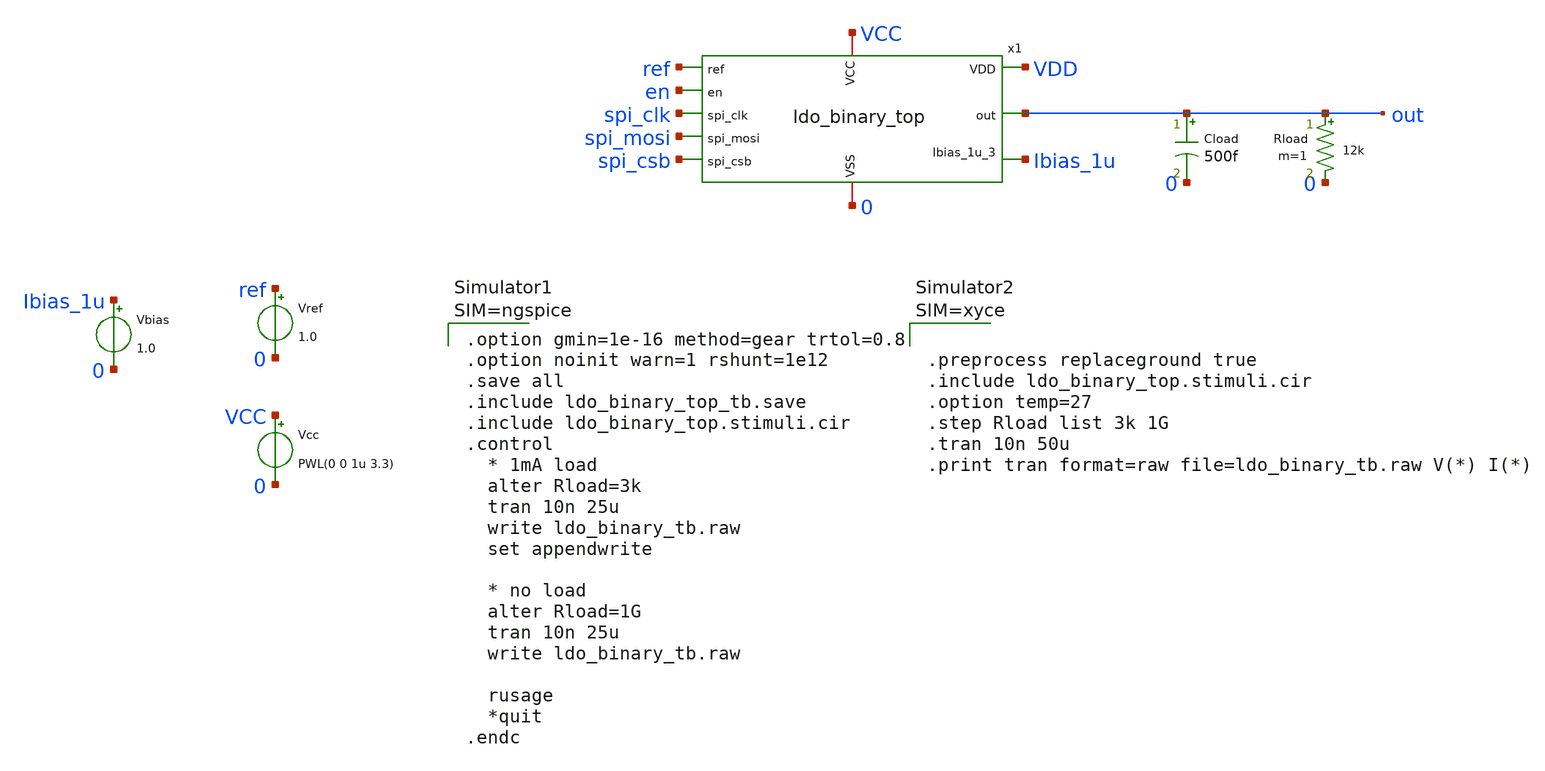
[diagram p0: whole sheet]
** sch_path: FLDO/design_data/xschem/ldo_binary_top_tb.sch
* IHP-GmbH/IHP-Open-PDK/ihp-sg13g2/libs.tech/xschem/sg13g2_stdcells/sg13g2_decap_4.sch:
* Copyright 2023 IHP PDK Authors
* Licensed under the Apache License, Version 2.0 (the "License");
**.subckt ldo_binary_top_tb
x1 VCC 0 spi_clk spi_mosi spi_csb ref en out Ibias_1u VDD ldo_binary_top
Vcc VCC 0 PWL(0 0 1u 3.3)
Vref ref 0 1.0
Cload out 0 500f m=1
Rload out 0 12k m=1
Vbias Ibias_1u 0 1.0
**** begin user architecture code









** IHP models
.lib cornerMOSlv.lib mos_tt
.lib cornerMOShv.lib mos_tt
.lib cornerHBT.lib hbt_typ
.lib cornerRES.lib res_typ
.lib cornerCAP.lib cap_typ

.include sg13g2_stdcell.spice






.option gmin=1e-16 method=gear trtol=0.8
.option noinit warn=1 rshunt=1e12
.save all
.include ldo_binary_top_tb.save
.include ldo_binary_top.stimuli.cir
.control
  * 1mA load
  alter Rload=3k
  tran 10n 25u
  write ldo_binary_tb.raw
  set appendwrite

  * no load
  alter Rload=1G
  tran 10n 25u
  write ldo_binary_tb.raw

  rusage
  *quit
.endc



**** end user architecture code
**.ends

* expanding   symbol:  ldo_binary_top.sym # of pins=10
** sym_path: FLDO/design_data/xschem/ldo_binary_top.sym
** sch_path: FLDO/design_data/xschem/ldo_binary_top.sch
.subckt ldo_binary_top VCC VSS spi_clk spi_mosi spi_csb ref en out Ibias_1u_3 VDD
*.iopin VCC
*.ipin spi_clk
*.iopin VSS
*.opin out
*.ipin spi_mosi
*.ipin spi_csb
*.ipin ref
*.ipin en
*.opin Ibias_1u_3
*.opin VDD
x_shift3 VCC VDD VSS a3 a3_hv shifter
x_shift2 VCC VDD VSS a2 a2_hv shifter
x_shift1 VCC VDD VSS a1 a1_hv shifter
x_shift0 VCC VDD VSS a0 a0_hv shifter
x1 VCC VSS ref Ibias_1u_1 out a3_hv a2_hv a1_hv a0_hv net1 ldo_binary
x3 VCC VSS ref Ibias_1u_2 VDD por ldo_1v2
x4 VCC VSS Ibias_1u_1 Ibias_1u_2 Ibias_1u_3 por biasgen
x2 VDD VSS spi_clk spi_mosi spi_csb por en a3 a2 a1 a0 en_ldo_n ldo_control
x_shift_enable VCC VDD VSS en_ldo_n net1 shifter
.ends


* expanding   symbol:  shifter.sym # of pins=5
** sym_path: FLDO/design_data/xschem/shifter.sym
** sch_path: FLDO/design_data/xschem/shifter.sch
.subckt shifter VDD_3v3 VDD_1v2 GND in out
*.iopin VDD_3v3
*.iopin VDD_1v2
*.iopin GND
*.ipin in
*.opin out
XM1 lvlsh in_b GND GND sg13_hv_nmos w=2u l=0.45u ng=1 m=1 mm_ok=1
XM2 lvlsh_b in GND GND sg13_hv_nmos w=2u l=0.45u ng=1 m=1 mm_ok=1
XM3 lvlsh lvlsh_b VDD_3v3 VDD_3v3 sg13_hv_pmos w=0.3u l=0.45u ng=1 m=1 mm_ok=1
XM4 lvlsh_b lvlsh VDD_3v3 VDD_3v3 sg13_hv_pmos w=0.3u l=0.45u ng=1 m=1 mm_ok=1
XM5 in_b in GND GND sg13_lv_nmos w=0.74u l=0.13u ng=1 m=1 mm_ok=1
XM6 in_b in VDD_1v2 VDD_1v2 sg13_lv_pmos w=1.12u l=0.13u ng=1 m=1 mm_ok=1
XM7 out lvlsh_b GND GND sg13_hv_nmos w=2u l=0.45u ng=1 m=1 mm_ok=1
XM8 out lvlsh_b VDD_3v3 VDD_3v3 sg13_hv_pmos w=2u l=0.4u ng=1 m=2 mm_ok=1
.ends


* expanding   symbol:  ldo_binary.sym # of pins=7
** sym_path: FLDO/design_data/xschem/ldo_binary.sym
** sch_path: FLDO/design_data/xschem/ldo_binary.sch
.subckt ldo_binary VCC GND ref Ibias_1u out a3 a2 a1 a0 en_n
*.iopin VCC
*.iopin GND
*.ipin ref
*.ipin Ibias_1u
*.opin out
*.ipin a3,a2,a1,a0
*.ipin en_n
XR4 net1 out GND rhigh w=0.5e-6 l=12e-6 m=1 b=0
XM1 net1 a0 out VCC sg13_hv_pmos w=2u l=0.4u ng=1 m=1 mm_ok=1
XM2 net2 a1 net1 VCC sg13_hv_pmos w=2u l=0.4u ng=1 m=1 mm_ok=1
XM3 net3 a2 net2 VCC sg13_hv_pmos w=2u l=0.4u ng=1 m=1 mm_ok=1
XM4 out vg net4 net4 sg13_hv_pmos w=100u l=0.4u ng=10 m=1 mm_ok=1
Vmeas VCC net4 0
.save i(vmeas)
XC1 out vg cap_cmim w=10.0e-6 l=10.0e-6 m=1
XM11 net5 a3 net3 VCC sg13_hv_pmos w=2u l=0.4u ng=1 m=1 mm_ok=1
XM15 vg en VCC VCC sg13_hv_pmos w=0.3u l=0.4u ng=1 m=1 mm_ok=1
x1 VCC GND Ibias_1u fb ref vg ldo_ota
XM5 Ibias_1u en_n GND GND sg13_hv_nmos w=0.3u l=0.45u ng=1 m=1 mm_ok=1
XM6 en en_n GND GND sg13_hv_nmos w=0.3u l=0.45u ng=1 m=1 mm_ok=1
XM7 en en_n VCC VCC sg13_hv_pmos w=0.3u l=0.4u ng=1 m=1 mm_ok=1
XRdummy GND GND gnd rhigh w=0.5e-6 l=12e-6 m=5 b=0
XR2 net2 net1 GND rhigh w=0.5e-6 l=2*12e-6 m=1 b=0
XR6 net3 net2 GND rhigh w=0.5e-6 l=4*12e-6 m=1 b=0
XR5 net5 net3 GND rhigh w=0.5e-6 l=8*12e-6 m=1 b=0
XR3 fb net5 GND rhigh w=0.5e-6 l=6*12e-6 m=1 b=0
XR1 GND fb GND rhigh w=0.5e-6 l=10*12e-6 m=1 b=0
.ends


* expanding   symbol:  ldo_1v2.sym # of pins=6
** sym_path: FLDO/design_data/xschem/ldo_1v2.sym
** sch_path: FLDO/design_data/xschem/ldo_1v2.sch
.subckt ldo_1v2 VCC GND ref Ibias_1u out en_n
*.iopin VCC
*.iopin GND
*.ipin ref
*.ipin Ibias_1u
*.opin out
*.ipin en_n
XM4 out vg net1 net1 sg13_hv_pmos w=50u l=0.4u ng=10 m=1 mm_ok=1
Vmeas VCC net1 0
.save i(vmeas)
XC1 out vg cap_cmim w=10.0e-6 l=10.0e-6 m=1
XM2 Ibias_1u en_n GND GND sg13_hv_nmos w=0.3u l=0.45u ng=1 m=1 mm_ok=1
XM3 vg en VCC VCC sg13_hv_pmos w=0.3u l=0.4u ng=1 m=1 mm_ok=1
XM1 en en_n GND GND sg13_hv_nmos w=0.3u l=0.45u ng=1 m=1 mm_ok=1
XM11 en en_n VCC VCC sg13_hv_pmos w=0.3u l=0.4u ng=1 m=1 mm_ok=1
XRdummy GND GND gnd rhigh w=0.5e-6 l=4e-6 m=2 b=0 mm_ok=1
x1 VCC GND Ibias_1u fb ref vg ldo_ota
XR2 fb out gnd rhigh w=0.5e-6 l=4*4e-6 m=1 b=0
XR1 GND fb gnd rhigh w=0.5e-6 l=20*4e-6 m=1 b=0
.ends


* expanding   symbol:  biasgen.sym # of pins=4
** sym_path: FLDO/design_data/xschem/biasgen.sym
** sch_path: FLDO/design_data/xschem/biasgen.sch
.subckt biasgen VCC GND Ibias_1u_1 Ibias_1u_2 Ibias_1u_3 por
*.iopin VCC
*.iopin GND
*.iopin Ibias_1u_1,Ibias_1u_2,Ibias_1u_3
*.opin por
XM1 vp vn net1 GND sg13_hv_nmos w=2u l=2u ng=1 m=3 mm_ok=1
XM2 vn vn GND GND sg13_hv_nmos w=2u l=2u ng=1 m=1 mm_ok=1
XM3 vn vp VCC VCC sg13_hv_pmos w=0.5u l=2u ng=1 m=2 mm_ok=1
XM4 vp vp VCC VCC sg13_hv_pmos w=0.5u l=2u ng=1 m=2 mm_ok=1
XMout0 Ibias_1u_0 vp VCC VCC sg13_hv_pmos w=0.5u l=2u ng=1 m=1 mm_ok=1
XMout1 Ibias_1u_1 vp VCC VCC sg13_hv_pmos w=0.5u l=2u ng=1 m=1 mm_ok=1
XMout2 Ibias_1u_2 vp VCC VCC sg13_hv_pmos w=0.5u l=2u ng=1 m=1 mm_ok=1
XMout3 Ibias_1u_3 vp VCC VCC sg13_hv_pmos w=0.5u l=2u ng=1 m=1 mm_ok=1
XC1 Ibias_1u_0 GND cap_cmim w=7.0e-6 l=7.0e-6 m=1
XM7 por Ibias_1u_0 VCC VCC sg13_hv_pmos w=0.3u l=0.4u ng=1 m=1 mm_ok=1
XM8 por Ibias_1u_0 GND GND sg13_hv_nmos w=0.3u l=0.45u ng=1 m=1 mm_ok=1
XR1 net1 GND GND rppd w=0.5e-6 l=80e-6 m=1 b=0 mm_ok=1
XM5 vp vstart GND GND sg13_hv_nmos w=0.3u l=0.45u ng=1 m=1 mm_ok=1
XM6 vstart vn GND GND sg13_hv_nmos w=0.3u l=0.45u ng=1 m=1 mm_ok=1
XM9 vstart vn net2 VCC sg13_hv_pmos w=0.3u l=2u ng=1 m=1 mm_ok=1
XM10 net2 net2 net3 VCC sg13_hv_pmos w=0.3u l=2u ng=1 m=1 mm_ok=1
XM11 net3 net3 VCC VCC sg13_hv_pmos w=0.3u l=2u ng=1 m=1 mm_ok=1
.ends


* expanding   symbol:  ldo_control.sym # of pins=9
** sym_path: FLDO/design_data/xschem/ldo_control.sym
** sch_path: FLDO/design_data/xschem/ldo_control.sch
.subckt ldo_control VDD VSS spi_clk spi_di spi_ce por en data3 data2 data1 data0 en_ldo_n
*.iopin VDD
*.ipin spi_clk
*.iopin VSS
*.opin data3,data2,data1,data0
*.ipin spi_di
*.ipin spi_ce
*.ipin por
*.ipin en
*.opin en_ldo_n
x1 VDD VSS spi_clk spi_di spi_ce rst_b data3 data2 data1 data0 spi_register
x2 en_ldo_n rst_b en VDD VSS sg13g2_nand2_1
x3 rst_b por VDD VSS shifter_down_invert
x4 VDD VSS sg13g2_decap_4
x5 VDD VSS sg13g2_decap_4
x6 VDD VSS sg13g2_decap_8
x7 VDD VSS sg13g2_decap_8
x8 VDD VSS sg13g2_decap_8
x9 VDD VSS sg13g2_fill_2
.ends


* expanding   symbol:  ldo_ota.sym # of pins=6
** sym_path: FLDO/design_data/xschem/ldo_ota.sym
** sch_path: FLDO/design_data/xschem/ldo_ota.sch
.subckt ldo_ota VCC GND Ibias_1u plus min out
*.iopin VCC
*.iopin GND
*.ipin plus
*.ipin min
*.opin out
*.ipin Ibias_1u
XM5 vbp plus tail GND sg13_hv_nmos w=3u l=2u ng=3 m=1 mm_ok=1
XM6 out min tail GND sg13_hv_nmos w=3u l=2u ng=3 m=1 mm_ok=1
XM7 tail Ibias_1u GND GND sg13_hv_nmos w=1u l=2u ng=1 m=2 mm_ok=1
XM8 Ibias_1u Ibias_1u GND GND sg13_hv_nmos w=1u l=2u ng=1 m=1 mm_ok=1
XM9 out vbp VCC VCC sg13_hv_pmos w=2u l=2u ng=2 m=1 mm_ok=1
XM10 vbp vbp VCC VCC sg13_hv_pmos w=2u l=2u ng=2 m=1 mm_ok=1
XMdummy0 GND Ibias_1u GND GND sg13_hv_nmos w=1u l=2u ng=1 m=2 mm_ok=1
XMdummy1 tail tail tail GND sg13_hv_nmos w=1u l=2u ng=1 m=4 mm_ok=1
XMdummyP VCC vbp VCC VCC sg13_hv_pmos w=1u l=2u ng=1 m=2 mm_ok=1
.ends


* expanding   symbol:  spi_register.sym # of pins=7
** sym_path: FLDO/design_data/xschem/spi_register.sym
** sch_path: FLDO/design_data/xschem/spi_register.sch
.subckt spi_register VDD VSS spi_clk spi_di spi_ce rst_b data3 data2 data1 data0
*.iopin VDD
*.ipin spi_clk
*.iopin VSS
*.opin data3,data2,data1,data0
*.ipin spi_di
*.ipin spi_ce
*.ipin rst_b
xshift3 shiftreg3 net2[3] net1 shiftreg2 rst_b VDD VSS sg13g2_dfrbp_1
xshift2 shiftreg2 net2[2] net1 shiftreg1 rst_b VDD VSS sg13g2_dfrbp_1
xshift1 shiftreg1 net2[1] net1 shiftreg0 rst_b VDD VSS sg13g2_dfrbp_1
xshift0 shiftreg0 net2[0] net1 spi_di rst_b VDD VSS sg13g2_dfrbp_1
x2 net1 spi_clk spi_ce VDD VSS sg13g2_nor2_1
xdata3 shiftreg3 rst_b VGND VNB VPB VPWR data3 sg13g2_dlhrq_1
xdata2 shiftreg2 rst_b VGND VNB VPB VPWR data2 sg13g2_dlhrq_1
xdata1 shiftreg1 rst_b VGND VNB VPB VPWR data1 sg13g2_dlhrq_1
xdata0 shiftreg0 rst_b VGND VNB VPB VPWR data0 sg13g2_dlhrq_1
* noconn #net2
.ends


* expanding   symbol:  sg13g2_stdcells/sg13g2_nand2_1.sym # of pins=3
** sym_path: sg13g2_stdcells/sg13g2_nand2_1.sym
** sch_path: sg13g2_stdcells/sg13g2_nand2_1.sch
.subckt sg13g2_nand2_1 Y A B VDD VSS
*.iopin VDD
*.iopin VSS
*.ipin A
*.ipin B
*.opin Y
XM1 Y A net1 VSS sg13_lv_nmos w=740.00n l=130.00n ng=1 m=1 mm_ok=1
XM2 net1 B VSS VSS sg13_lv_nmos w=740.00n l=130.00n ng=1 m=1 mm_ok=1
XM3 Y A VDD VDD sg13_lv_pmos w=1.12u l=130.00n ng=1 m=1 mm_ok=1
XM4 Y B VDD VDD sg13_lv_pmos w=1.12u l=130.00n ng=1 m=1 mm_ok=1
.ends


* expanding   symbol:  shifter_down_invert.sym # of pins=2
** sym_path: FLDO/design_data/xschem/shifter_down_invert.sym
** sch_path: FLDO/design_data/xschem/shifter_down_invert.sch
.subckt shifter_down_invert Y A VDD VSS
*.opin Y
*.ipin A
XM1 Y A VSS VSS sg13_hv_nmos w=0.3u l=0.45u ng=1 m=1 mm_ok=1
XM2 Y A VDD VDD sg13_hv_pmos w=0.3u l=0.4u ng=1 m=1 mm_ok=1
.ends


* expanding   symbol:  sg13g2_stdcells/sg13g2_decap_4.sym # of pins=0
** sym_path: sg13g2_stdcells/sg13g2_decap_4.sym
** sch_path: sg13g2_stdcells/sg13g2_decap_4.sch
.subckt sg13g2_decap_4 VDD VSS
*.iopin VDD
*.iopin VSS
XM1 VSS VDD VSS VSS sg13_lv_nmos w=420.00n l=1.000u ng=1 m=1 mm_ok=1
XM2 VDD VSS VDD VDD sg13_lv_pmos w=1.000u l=1.000u ng=1 m=1 mm_ok=1
.ends


* expanding   symbol:  sg13g2_stdcells/sg13g2_decap_8.sym # of pins=0
** sym_path: sg13g2_stdcells/sg13g2_decap_8.sym
** sch_path: sg13g2_stdcells/sg13g2_decap_8.sch
.subckt sg13g2_decap_8 VDD VSS
*.iopin VDD
*.iopin VSS
XM1 VSS VDD VSS VSS sg13_lv_nmos w=840.00n l=1.000u ng=2 m=1 mm_ok=1
XM2 VDD VSS VDD VDD sg13_lv_pmos w=2.000u l=1.000u ng=2 m=1 mm_ok=1
.ends


* expanding   symbol:  sg13g2_stdcells/sg13g2_fill_2.sym # of pins=0
** sym_path: sg13g2_stdcells/sg13g2_fill_2.sym
** sch_path: sg13g2_stdcells/sg13g2_fill_2.sch
.subckt sg13g2_fill_2 VDD VSS
*.iopin VDD
*.iopin VSS
.ends


* expanding   symbol:  sg13g2_stdcells/sg13g2_dfrbp_1.sym # of pins=5
** sym_path: sg13g2_stdcells/sg13g2_dfrbp_1.sym
** sch_path: sg13g2_stdcells/sg13g2_dfrbp_1.sch
.subckt sg13g2_dfrbp_1 Q Q_N CLK D RESET_B VDD VSS
*.ipin D
*.ipin RESET_B
*.ipin CLK
*.opin Q
*.opin Q_N
*.iopin VDD
*.iopin VSS
XM1 Db D net10 VSS sg13_lv_nmos w=420.00n l=130.00n ng=1 m=1 mm_ok=1
XM2 net10 RESET_B VSS VSS sg13_lv_nmos w=420.00n l=130.00n ng=1 m=1 mm_ok=1
XM3 net1 clkneg net9 VSS sg13_lv_nmos w=420.00n l=130.00n ng=1 m=1 mm_ok=1
XM4 net9 net1 VSS VSS sg13_lv_nmos w=420.00n l=130.00n ng=1 m=1 mm_ok=1
XM5 net1 net1 net5 VSS sg13_lv_nmos w=420.00n l=130.00n ng=1 m=1 mm_ok=1
XM6 net5 RESET_B VSS VSS sg13_lv_nmos w=420.00n l=130.00n ng=1 m=1 mm_ok=1
XM7 Q_N net1 VSS VSS sg13_lv_nmos w=740.00n l=130.00n ng=1 m=1 mm_ok=1
XM8 net2 net1 VSS VSS sg13_lv_nmos w=740.00n l=130.00n ng=1 m=1 mm_ok=1
XM9 Q net2 VSS VSS sg13_lv_nmos w=740.00n l=130.00n ng=1 m=1 mm_ok=1
XM10 clkneg CLK VSS VSS sg13_lv_nmos w=740.00n l=130.00n ng=1 m=1 mm_ok=1
XM11 clkpos clkneg VSS VSS sg13_lv_nmos w=740.00n l=130.00n ng=1 m=1 mm_ok=1
XM12 Db clkneg net3 VSS sg13_lv_nmos w=420.00n l=130.00n ng=1 m=1 mm_ok=1
XM13 net3 clkpos net8 VSS sg13_lv_nmos w=420.00n l=130.00n ng=1 m=1 mm_ok=1
XM14 net8 net3 net4 VSS sg13_lv_nmos w=420.00n l=130.00n ng=1 m=1 mm_ok=1
XM15 net4 RESET_B VSS VSS sg13_lv_nmos w=420.00n l=130.00n ng=1 m=1 mm_ok=1
XM16 net3 net3 VSS VSS sg13_lv_nmos w=740.00n l=130.00n ng=1 m=1 mm_ok=1
XM17 net3 clkpos net1 VSS sg13_lv_nmos w=740.00n l=130.00n ng=1 m=1 mm_ok=1
XM18 Db RESET_B VDD VDD sg13_lv_pmos w=420.00n l=130.00n ng=1 m=1 mm_ok=1
XM19 Db D VDD VDD sg13_lv_pmos w=420.00n l=130.00n ng=1 m=1 mm_ok=1
XM20 net7 net1 VDD VDD sg13_lv_pmos w=420.00n l=130.00n ng=1 m=1 mm_ok=1
XM21 net1 clkpos net7 VDD sg13_lv_pmos w=420.00n l=130.00n ng=1 m=1 mm_ok=1
XM22 net1 net1 VDD VDD sg13_lv_pmos w=420.00n l=130.00n ng=1 m=1 mm_ok=1
XM23 net1 RESET_B VDD VDD sg13_lv_pmos w=420.00n l=130.00n ng=1 m=1 mm_ok=1
XM24 Q_N net1 VDD VDD sg13_lv_pmos w=1.12u l=130.00n ng=1 m=1 mm_ok=1
XM25 net2 net1 VDD VDD sg13_lv_pmos w=1.12u l=130.00n ng=1 m=1 mm_ok=1
XM26 Q net2 VDD VDD sg13_lv_pmos w=1.12u l=130.00n ng=1 m=1 mm_ok=1
XM27 clkneg CLK VDD VDD sg13_lv_pmos w=1.12u l=130.00n ng=1 m=1 mm_ok=1
XM28 clkpos clkneg VDD VDD sg13_lv_pmos w=1.12u l=130.00n ng=1 m=1 mm_ok=1
XM29 Db clkpos net3 VDD sg13_lv_pmos w=420.00n l=130.00n ng=1 m=1 mm_ok=1
XM30 net6 net3 VDD VDD sg13_lv_pmos w=420.00n l=130.00n ng=1 m=1 mm_ok=1
XM31 net3 clkneg net6 VDD sg13_lv_pmos w=420.00n l=130.00n ng=1 m=1 mm_ok=1
XM32 net3 RESET_B VDD VDD sg13_lv_pmos w=420.00n l=130.00n ng=1 m=1 mm_ok=1
XM33 net3 net3 VDD VDD sg13_lv_pmos w=1.000u l=130.00n ng=1 m=1 mm_ok=1
XM34 net3 clkneg net1 VDD sg13_lv_pmos w=1.000u l=130.00n ng=1 m=1 mm_ok=1
.ends


* expanding   symbol:  sg13g2_stdcells/sg13g2_nor2_1.sym # of pins=3
** sym_path: sg13g2_stdcells/sg13g2_nor2_1.sym
** sch_path: sg13g2_stdcells/sg13g2_nor2_1.sch
.subckt sg13g2_nor2_1 Y A B VDD VSS
*.opin Y
*.ipin B
*.ipin A
*.iopin VDD
*.iopin VSS
XM1 Y A VSS VSS sg13_lv_nmos w=740.00n l=130.00n ng=1 m=1 mm_ok=1
XM2 Y B VSS VSS sg13_lv_nmos w=740.00n l=130.00n ng=1 m=1 mm_ok=1
XM3 net1 A VDD VDD sg13_lv_pmos w=1.12u l=130.00n ng=1 m=1 mm_ok=1
XM4 Y B net1 VDD sg13_lv_pmos w=1.12u l=130.00n ng=1 m=1 mm_ok=1
.ends

.end
